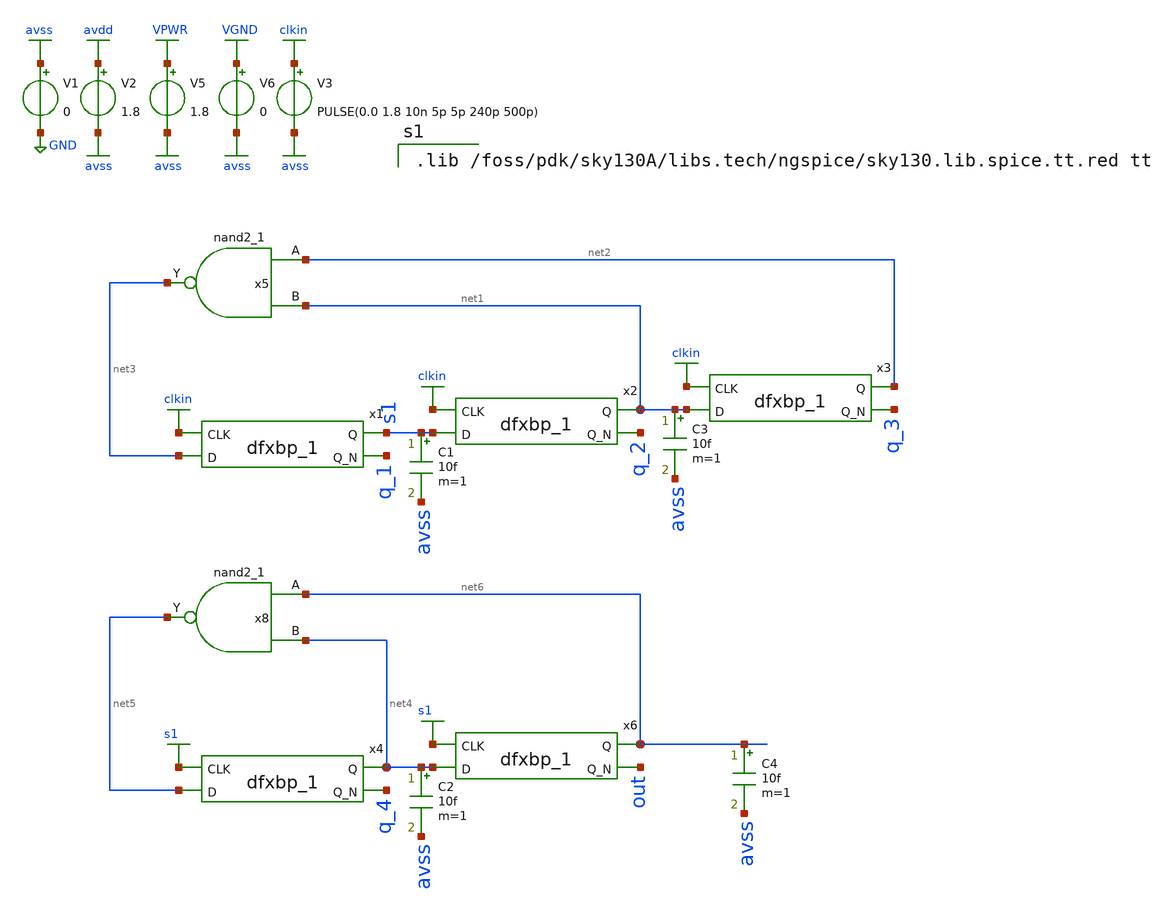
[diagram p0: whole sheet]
** sch_path: xschem/d_ff_sim8.sch
**.subckt d_ff_sim8
V1 avss GND 0
V2 avdd avss 1.8
V3 clkin avss PULSE(0.0 1.8 10n 5p 5p 240p 500p)
V5 VPWR avss 1.8
V6 VGND avss 0
x1 clkin net3 VGND VNB VPB VPWR s1 q_1 sky130_fd_sc_hd__dfxbp_1
x2 clkin s1 VGND VNB VPB VPWR net1 q_2 sky130_fd_sc_hd__dfxbp_1
C1 s1 avss 10f m=1
x3 clkin net1 VGND VNB VPB VPWR net2 q_3 sky130_fd_sc_hd__dfxbp_1
x5 net2 net1 VGND VNB VPB VPWR net3 sky130_fd_sc_hd__nand2_1
C3 net1 avss 10f m=1
x4 s1 net5 VGND VNB VPB VPWR net4 q_4 sky130_fd_sc_hd__dfxbp_1
x6 s1 net4 VGND VNB VPB VPWR net6 out sky130_fd_sc_hd__dfxbp_1
C2 net4 avss 10f m=1
x8 net6 net4 VGND VNB VPB VPWR net5 sky130_fd_sc_hd__nand2_1
C4 net6 avss 10f m=1
**** begin user architecture code

.lib /foss/pdk/sky130A/libs.tech/ngspice/sky130.lib.spice.tt.red tt



.include /foss/pdk/sky130A/libs.ref/sky130_fd_sc_hd/spice/sky130_fd_sc_hd.spice
.control
set temp=25
save clkin s1 out @V1[i] @V3[i] @V5[i]
tran 0.05n 200n 0n
plot @V1[i] @V3[i] @V5[i]
plot clkin out
plot out
fft clkin s1 out
plot db(mag(clkin)) db(mag(s1)) db(mag(out)) xlimit 0.0meg 5g ylimit 0.0 -120
.endc
.end


**** end user architecture code
**.ends
.GLOBAL avdd
.GLOBAL avss
.GLOBAL GND
.GLOBAL clkin
.GLOBAL VPWR
.GLOBAL VGND
.GLOBAL s1
.end
